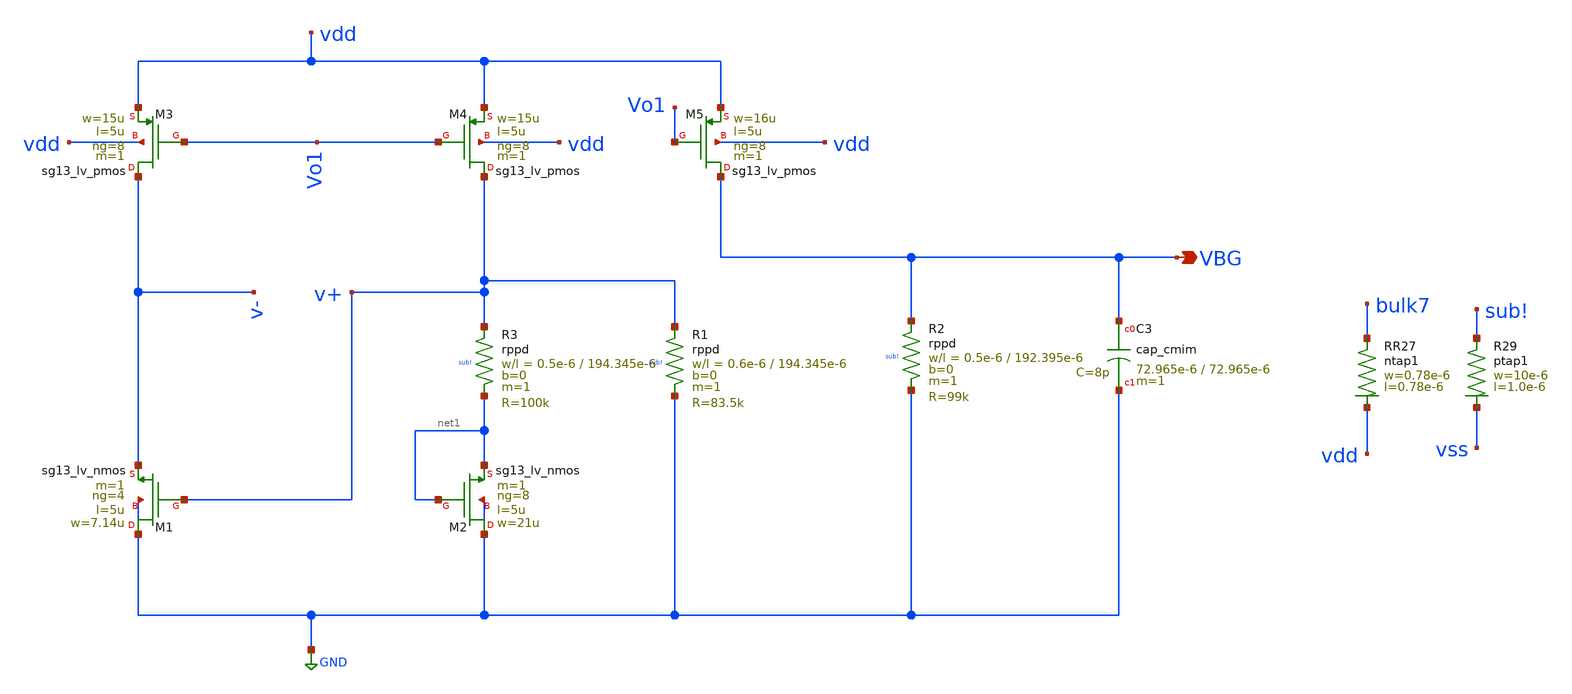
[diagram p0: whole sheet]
** sch_path: modules/module_1_bandgap_reference/part_3_layout/BGR_layout/bandgap_core/schematic_mod/bandgap_reference.sch
**.subckt bandgap_reference VBG
*.opin VBG
XM1 GND v+ v- GND sg13_lv_nmos w=7.14u l=5u ng=4 m=1 mm_ok=1
XM2 GND net1 net1 GND sg13_lv_nmos w=21u l=5u ng=8 m=1 mm_ok=1
XM3 v- Vo1 vdd vdd sg13_lv_pmos w=15u l=5u ng=8 m=1 mm_ok=1
XM4 v+ Vo1 vdd vdd sg13_lv_pmos w=15u l=5u ng=8 m=1 mm_ok=1
XM5 VBG Vo1 vdd vdd sg13_lv_pmos w=16u l=5u ng=8 m=1 mm_ok=1
XC3 VBG GND cap_cmim w=72.965e-6 l=72.965e-6 m=1 mm_ok=1
XR3 v+ net1 sub! rppd w=0.5e-6 l=194.345e-6 m=1 b=0 mm_ok=1
XR1 v+ GND sub! rppd w=0.6e-6 l=194.345e-6 m=1 b=0 mm_ok=1
XR2 VBG GND sub! rppd w=0.5e-6 l=192.395e-6 m=1 b=0 mm_ok=1
XR27 bulk7 vdd ntap1 R=262.8 w=0.78e-6 l=0.78e-6
XR29 sub! vss ptap1 R=30.62 w=10e-6 l=1.0e-6
**.ends
.GLOBAL GND
.end
